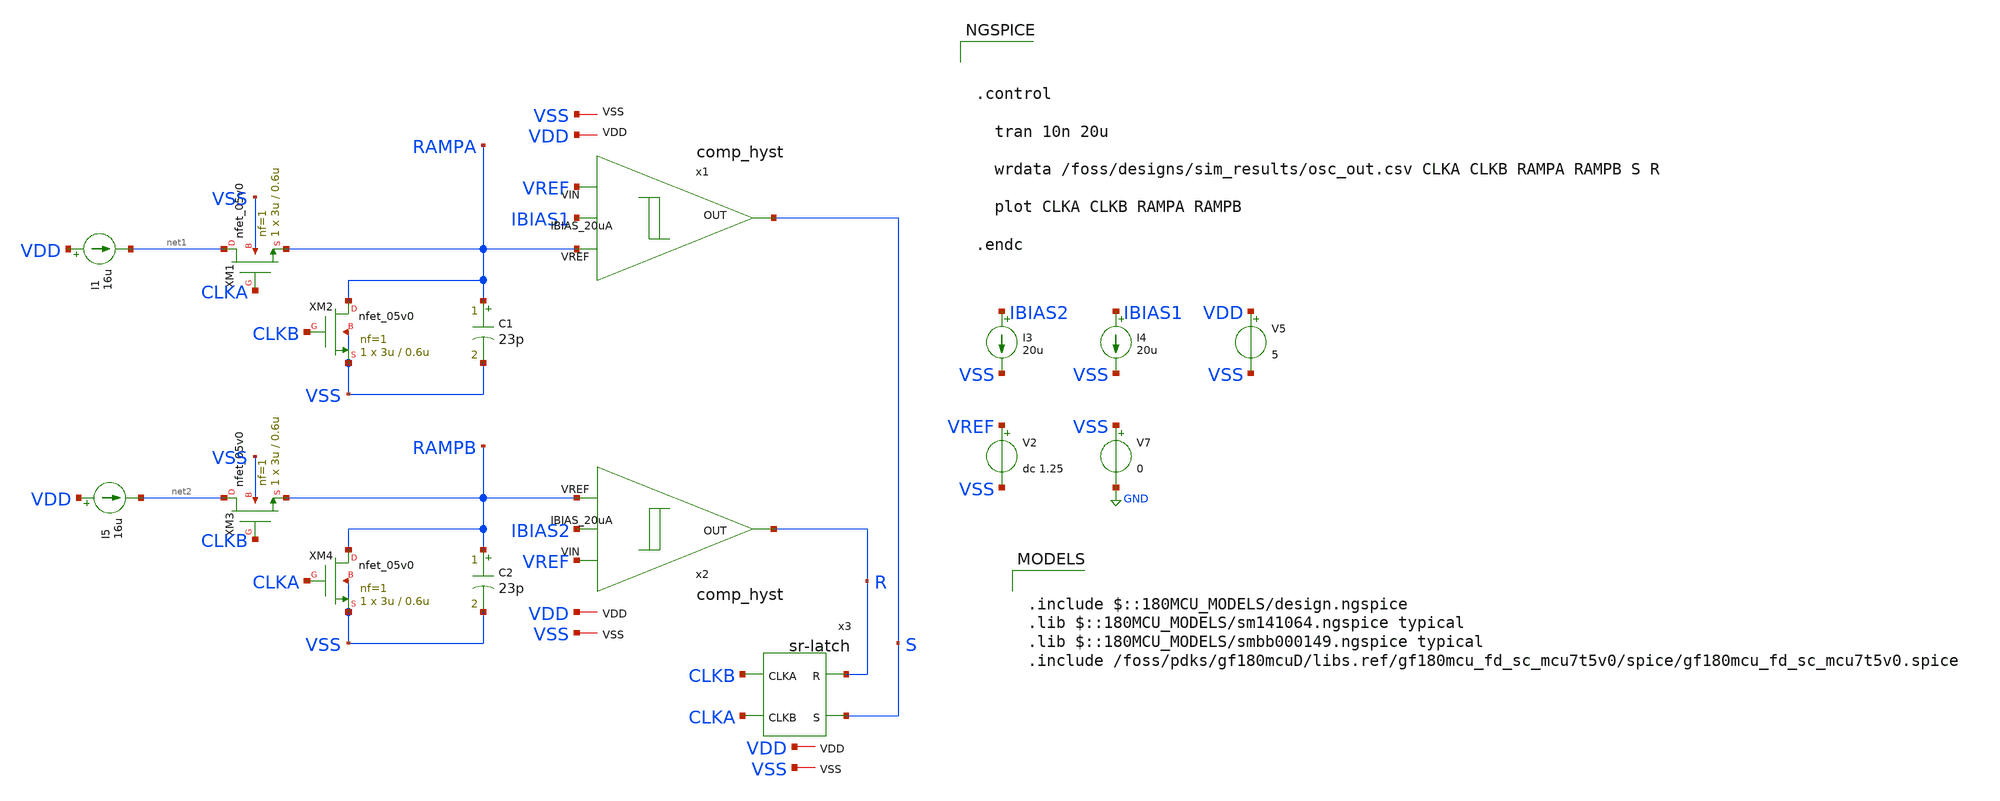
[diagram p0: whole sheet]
** sch_path: designs/relaxation-oscillator/relaxation-oscillator.sch
**.subckt relaxation-oscillator
XM1 net1 CLKA RAMPA VSS nfet_05v0 L=0.6u W=3u nf=1 ad='int((nf+1)/2) * W/nf * 0.18u' as='int((nf+2)/2) * W/nf * 0.18u'
+ pd='2*int((nf+1)/2) * (W/nf + 0.18u)' ps='2*int((nf+2)/2) * (W/nf + 0.18u)' nrd='0.18u / W' nrs='0.18u / W'
+ sa=0 sb=0 sd=0 m=1
XM2 RAMPA CLKB VSS VSS nfet_05v0 L=0.6u W=3u nf=1 ad='int((nf+1)/2) * W/nf * 0.18u' as='int((nf+2)/2) * W/nf * 0.18u'
+ pd='2*int((nf+1)/2) * (W/nf + 0.18u)' ps='2*int((nf+2)/2) * (W/nf + 0.18u)' nrd='0.18u / W' nrs='0.18u / W'
+ sa=0 sb=0 sd=0 m=1
C1 RAMPA VSS 23p m=1
XM3 net2 CLKB RAMPB VSS nfet_05v0 L=0.6u W=3u nf=1 ad='int((nf+1)/2) * W/nf * 0.18u' as='int((nf+2)/2) * W/nf * 0.18u'
+ pd='2*int((nf+1)/2) * (W/nf + 0.18u)' ps='2*int((nf+2)/2) * (W/nf + 0.18u)' nrd='0.18u / W' nrs='0.18u / W'
+ sa=0 sb=0 sd=0 m=1
XM4 RAMPB CLKA VSS VSS nfet_05v0 L=0.6u W=3u nf=1 ad='int((nf+1)/2) * W/nf * 0.18u' as='int((nf+2)/2) * W/nf * 0.18u'
+ pd='2*int((nf+1)/2) * (W/nf + 0.18u)' ps='2*int((nf+2)/2) * (W/nf + 0.18u)' nrd='0.18u / W' nrs='0.18u / W'
+ sa=0 sb=0 sd=0 m=1
C2 RAMPB VSS 23p m=1
V2 VREF VSS dc 1.25
V5 VDD VSS 5
V7 VSS GND 0
I4 IBIAS1 VSS 20u
I1 VDD net1 16u
I3 IBIAS2 VSS 20u
x1 VDD IBIAS1 VREF RAMPA S VSS comp_hyst
x2 VDD IBIAS2 VREF RAMPB R VSS comp_hyst
I5 VDD net2 16u
x3 VDD R CLKB S CLKA VSS sr-latch
**** begin user architecture code



.control

  tran 10n 20u

  wrdata /foss/designs/sim_results/osc_out.csv CLKA CLKB RAMPA RAMPB S R

  plot CLKA CLKB RAMPA RAMPB

.endc




.include $::180MCU_MODELS/design.ngspice
.lib $::180MCU_MODELS/sm141064.ngspice typical
.lib $::180MCU_MODELS/smbb000149.ngspice typical
.include /foss/pdks/gf180mcuD/libs.ref/gf180mcu_fd_sc_mcu7t5v0/spice/gf180mcu_fd_sc_mcu7t5v0.spice

**** end user architecture code
**.ends

* expanding   symbol:  /foss/designs/2026/buck-gf180-test/designs/hyst-comparator/comp_hyst.sym # of
*+ pins=6
** sym_path: designs/hyst-comparator/comp_hyst.sym
** sch_path: designs/hyst-comparator/comp_hyst.sch
.subckt comp_hyst VDD IBIAS_20uA VIN VREF OUT VSS
*.ipin VIN
*.ipin VREF
*.opin OUT
*.ipin IBIAS_20uA
*.iopin VDD
*.iopin VSS
XM1 net2 IBIAS_20uA VDD VDD pfet_05v0 L=1u W=11.8u nf=1 ad='int((nf+1)/2) * W/nf * 0.18u' as='int((nf+2)/2) * W/nf * 0.18u'
+ pd='2*int((nf+1)/2) * (W/nf + 0.18u)' ps='2*int((nf+2)/2) * (W/nf + 0.18u)' nrd='0.18u / W' nrs='0.18u / W'
+ sa=0 sb=0 sd=0 m=1
XM2 IBIAS_20uA IBIAS_20uA VDD VDD pfet_05v0 L=1u W=11.8u nf=1 ad='int((nf+1)/2) * W/nf * 0.18u' as='int((nf+2)/2) * W/nf * 0.18u'
+ pd='2*int((nf+1)/2) * (W/nf + 0.18u)' ps='2*int((nf+2)/2) * (W/nf + 0.18u)' nrd='0.18u / W' nrs='0.18u / W'
+ sa=0 sb=0 sd=0 m=1
XM3 net1 net1 VDD VDD pfet_05v0 L=1u W=11.8u nf=1 ad='int((nf+1)/2) * W/nf * 0.18u' as='int((nf+2)/2) * W/nf * 0.18u'
+ pd='2*int((nf+1)/2) * (W/nf + 0.18u)' ps='2*int((nf+2)/2) * (W/nf + 0.18u)' nrd='0.18u / W' nrs='0.18u / W'
+ sa=0 sb=0 sd=0 m=1
XM4 OUT net1 VDD VDD pfet_05v0 L=1u W=11.8u nf=1 ad='int((nf+1)/2) * W/nf * 0.18u' as='int((nf+2)/2) * W/nf * 0.18u'
+ pd='2*int((nf+1)/2) * (W/nf + 0.18u)' ps='2*int((nf+2)/2) * (W/nf + 0.18u)' nrd='0.18u / W' nrs='0.18u / W'
+ sa=0 sb=0 sd=0 m=1
XM5 net4 VIN net2 VDD pfet_05v0 L=1u W=11.21u nf=1 ad='int((nf+1)/2) * W/nf * 0.18u' as='int((nf+2)/2) * W/nf * 0.18u'
+ pd='2*int((nf+1)/2) * (W/nf + 0.18u)' ps='2*int((nf+2)/2) * (W/nf + 0.18u)' nrd='0.18u / W' nrs='0.18u / W'
+ sa=0 sb=0 sd=0 m=1
XM6 net3 VREF net2 VDD pfet_05v0 L=1u W=11.21u nf=1 ad='int((nf+1)/2) * W/nf * 0.18u' as='int((nf+2)/2) * W/nf * 0.18u'
+ pd='2*int((nf+1)/2) * (W/nf + 0.18u)' ps='2*int((nf+2)/2) * (W/nf + 0.18u)' nrd='0.18u / W' nrs='0.18u / W'
+ sa=0 sb=0 sd=0 m=1
XM7 net3 net3 VSS VSS nfet_05v0 L=1u W=6.78u nf=1 ad='int((nf+1)/2) * W/nf * 0.18u' as='int((nf+2)/2) * W/nf * 0.18u'
+ pd='2*int((nf+1)/2) * (W/nf + 0.18u)' ps='2*int((nf+2)/2) * (W/nf + 0.18u)' nrd='0.18u / W' nrs='0.18u / W'
+ sa=0 sb=0 sd=0 m=1
XM8 net4 net3 VSS VSS nfet_05v0 L=1u W=27.12u nf=1 ad='int((nf+1)/2) * W/nf * 0.18u' as='int((nf+2)/2) * W/nf * 0.18u'
+ pd='2*int((nf+1)/2) * (W/nf + 0.18u)' ps='2*int((nf+2)/2) * (W/nf + 0.18u)' nrd='0.18u / W' nrs='0.18u / W'
+ sa=0 sb=0 sd=0 m=1
XM9 net3 net4 VSS VSS nfet_05v0 L=1u W=27.12u nf=1 ad='int((nf+1)/2) * W/nf * 0.18u' as='int((nf+2)/2) * W/nf * 0.18u'
+ pd='2*int((nf+1)/2) * (W/nf + 0.18u)' ps='2*int((nf+2)/2) * (W/nf + 0.18u)' nrd='0.18u / W' nrs='0.18u / W'
+ sa=0 sb=0 sd=0 m=1
XM10 net4 net4 VSS VSS nfet_05v0 L=1u W=6.78u nf=1 ad='int((nf+1)/2) * W/nf * 0.18u' as='int((nf+2)/2) * W/nf * 0.18u'
+ pd='2*int((nf+1)/2) * (W/nf + 0.18u)' ps='2*int((nf+2)/2) * (W/nf + 0.18u)' nrd='0.18u / W' nrs='0.18u / W'
+ sa=0 sb=0 sd=0 m=1
XM11 net1 net4 VSS VSS nfet_05v0 L=1u W=6.78u nf=1 ad='int((nf+1)/2) * W/nf * 0.18u' as='int((nf+2)/2) * W/nf * 0.18u'
+ pd='2*int((nf+1)/2) * (W/nf + 0.18u)' ps='2*int((nf+2)/2) * (W/nf + 0.18u)' nrd='0.18u / W' nrs='0.18u / W'
+ sa=0 sb=0 sd=0 m=1
XM12 OUT net3 VSS VSS nfet_05v0 L=1u W=6.78u nf=1 ad='int((nf+1)/2) * W/nf * 0.18u' as='int((nf+2)/2) * W/nf * 0.18u'
+ pd='2*int((nf+1)/2) * (W/nf + 0.18u)' ps='2*int((nf+2)/2) * (W/nf + 0.18u)' nrd='0.18u / W' nrs='0.18u / W'
+ sa=0 sb=0 sd=0 m=1
.ends


* expanding   symbol:  sr-latch.sym # of pins=6
** sym_path: designs/relaxation-oscillator/sr-latch.sym
** sch_path: designs/relaxation-oscillator/sr-latch.sch
.subckt sr-latch VDD R CLKA S CLKB VSS
*.iopin VDD
*.iopin VSS
*.opin CLKA
*.opin CLKB
*.ipin R
*.ipin S
x1 VDD R CLKB CLKA VSS nor
x2 VDD CLKA S CLKB VSS nor
.ends


* expanding   symbol:  nor.sym # of pins=5
** sym_path: designs/relaxation-oscillator/nor.sym
** sch_path: designs/relaxation-oscillator/nor.sch
.subckt nor VDD A B OUT VSS
*.ipin A
*.ipin B
*.iopin VDD
*.iopin VSS
*.opin OUT
XM1 net1 A VDD VDD pfet_05v0 L=0.50u W=0.9u nf=1 ad='int((nf+1)/2) * W/nf * 0.18u' as='int((nf+2)/2) * W/nf * 0.18u'
+ pd='2*int((nf+1)/2) * (W/nf + 0.18u)' ps='2*int((nf+2)/2) * (W/nf + 0.18u)' nrd='0.18u / W' nrs='0.18u / W'
+ sa=0 sb=0 sd=0 m=1
XM2 OUT B net1 VDD pfet_05v0 L=0.50u W=0.9u nf=1 ad='int((nf+1)/2) * W/nf * 0.18u' as='int((nf+2)/2) * W/nf * 0.18u'
+ pd='2*int((nf+1)/2) * (W/nf + 0.18u)' ps='2*int((nf+2)/2) * (W/nf + 0.18u)' nrd='0.18u / W' nrs='0.18u / W'
+ sa=0 sb=0 sd=0 m=1
XM3 OUT A VSS VSS nfet_05v0 L=0.60u W=0.30u nf=1 ad='int((nf+1)/2) * W/nf * 0.18u' as='int((nf+2)/2) * W/nf * 0.18u'
+ pd='2*int((nf+1)/2) * (W/nf + 0.18u)' ps='2*int((nf+2)/2) * (W/nf + 0.18u)' nrd='0.18u / W' nrs='0.18u / W'
+ sa=0 sb=0 sd=0 m=1
XM4 OUT B VSS VSS nfet_05v0 L=0.60u W=0.30u nf=1 ad='int((nf+1)/2) * W/nf * 0.18u' as='int((nf+2)/2) * W/nf * 0.18u'
+ pd='2*int((nf+1)/2) * (W/nf + 0.18u)' ps='2*int((nf+2)/2) * (W/nf + 0.18u)' nrd='0.18u / W' nrs='0.18u / W'
+ sa=0 sb=0 sd=0 m=1
.ends

.GLOBAL GND
.end
